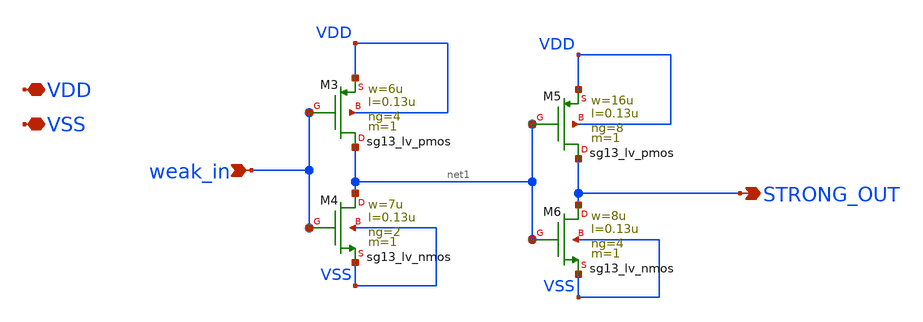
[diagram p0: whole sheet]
** sch_path: xschem/inverter_buffer.sch
**.subckt inverter_buffer VDD VSS weak_in STRONG_OUT
*.iopin VDD
*.iopin VSS
*.ipin weak_in
*.opin STRONG_OUT
XM3 net1 weak_in VDD VDD sg13_lv_pmos w=6u l=0.13u ng=4 m=1 mm_ok=1
XM4 net1 weak_in VSS VSS sg13_lv_nmos w=7u l=0.13u ng=2 m=1 mm_ok=1
XM5 STRONG_OUT net1 VDD VDD sg13_lv_pmos w=16u l=0.13u ng=8 m=1 mm_ok=1
XM6 STRONG_OUT net1 VSS VSS sg13_lv_nmos w=8u l=0.13u ng=4 m=1 mm_ok=1
**.ends
.end
